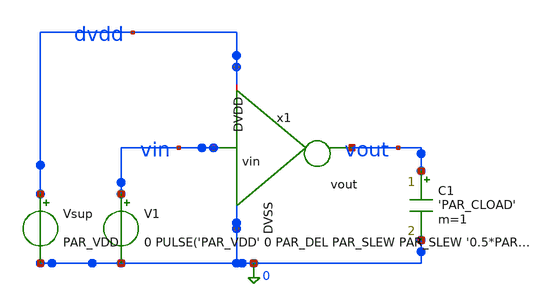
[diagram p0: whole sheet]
** sch_path: designs/emily_testing/TB_inv1.sch
**.subckt TB_inv1
V1 vin 0 0 PULSE('PAR_VDD' 0 PAR_DEL PAR_SLEW PAR_SLEW '0.5*PAR_PER' '1.0*PAR_PER')
Vsup dvdd 0 PAR_VDD
C1 vout 0 'PAR_CLOAD' m=1
**** begin user architecture code

.include $::180MCU_MODELS/design.ngspice
.lib $::180MCU_MODELS/sm141064.ngspice typical
.lib $::180MCU_MODELS/smbb000149.ngspice typical



** PARAMETERS
.PARAM PAR_VDD=3.3
.PARAM PAR_CLOAD=100f
.PARAM PAR_SLEW=100p
.PARAM PAR_PER=10n
.PARAM PAR_DEL='0.1*PAR_PER'

** Rise/Fall 10-90%
.MEASURE TRAN tr1090 TRIG v(vout) VAL='0.1*PAR_VDD' RISE=1 TARG v(vout) VAL='0.9*PAR_VDD' RISE=1
.MEASURE TRAN tf9010 TRIG v(vout) VAL='0.9*PAR_VDD' FALL=1 TARG v(vout) VAL='0.1*PAR_VDD' FALL=1

** Delay Rise Fall
.MEASURE TRAN tdrise TRIG v(vin)  VAL='0.5*PAR_VDD' FALL=1 TARG v(vout) VAL='0.5*PAR_VDD' RISE=1
.MEASURE TRAN tdfall TRIG v(vin)  VAL='0.5*PAR_VDD' RISE=1 TARG v(vout) VAL='0.5*PAR_VDD' FALL=1

**Leakage current and average current
.MEASURE TRAN iavg AVG vsup#branch FROM=PAR_DEL TO='PAR_DEL+PAR_PER'
.MEASURE TRAN ileak AVG vsup#branch FROM='PAR_DEL+0.4*PAR_PER' TO='PAR_DEL+0.45*PAR_PER'

.control
save all
OP
TRAN 1p 21n
write TB_inv1.raw
plot v(vin) v(vout)
.endc



**** end user architecture code
**.ends
.end
